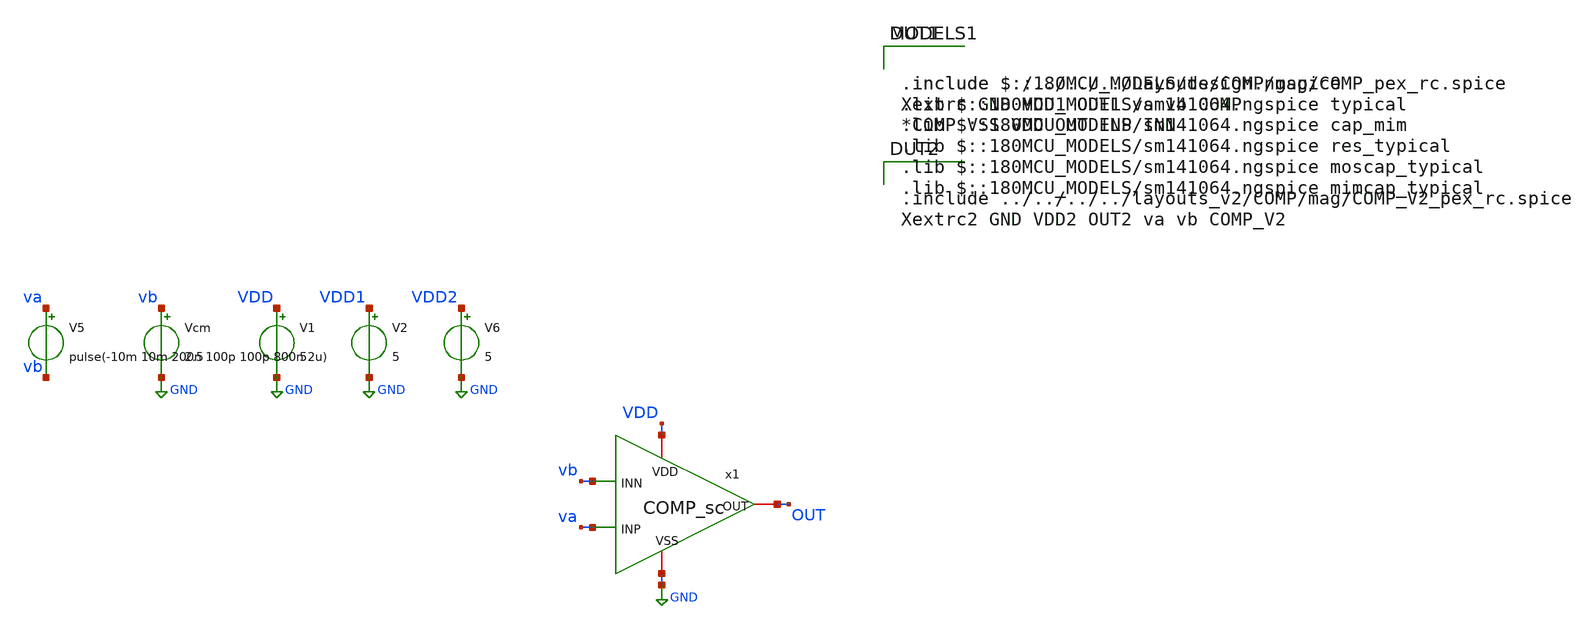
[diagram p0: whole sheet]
** sch_path: FINAL/XSCHEM/TEST/test_comp_tran.sch
**.subckt test_comp_tran
V1 VDD GND 5
V2 VDD1 GND 5
V5 va vb pulse(-10m 10m 200n 100p 100p 800n 2u)
Vcm vb GND 2.5
x1 VDD vb OUT va GND COMP_sc
V6 VDD2 GND 5
**** begin user architecture code

.include $::180MCU_MODELS/design.ngspice
.lib $::180MCU_MODELS/sm141064.ngspice typical
.lib $::180MCU_MODELS/sm141064.ngspice cap_mim
.lib $::180MCU_MODELS/sm141064.ngspice res_typical
.lib $::180MCU_MODELS/sm141064.ngspice moscap_typical
.lib $::180MCU_MODELS/sm141064.ngspice mimcap_typical


.include ../../../../Layouts/COMP/mag/COMP_pex_rc.spice
Xextrc GND VDD1 OUT1 va vb COMP
*COMP VSS VDD OUT INP INN


.include ../../../../layouts_v2/COMP/mag/COMP_V2_pex_rc.spice
Xextrc2 GND VDD2 OUT2 va vb COMP_V2



* CAREFUL: not one brace in this text. xschem counts them to find where the
* attribute block ends and a single one inside a comment cuts it in half,
* leaving the netlist with the template 'blabla' and raising no error.
*
* Transitorio de comparador, no de amplificador: lazo abierto y un escalon de
* overdrive of +-10 mV around the threshold. What is measured is the propagation
* delay -- from the input crossing to the half-rail crossing of the
* output -- and the rise and fall times, for the schematic and for the
* layout extraido.
* The threshold is zero because the measured COMP offset is tenths of a millivolt.
.save all
.control
tran 200p 2u
wrdata tran.txt v(va)-v(vb) v(OUT) v(OUT1) v(OUT2)
.endc


**** end user architecture code
**.ends
.GLOBAL GND
.end
